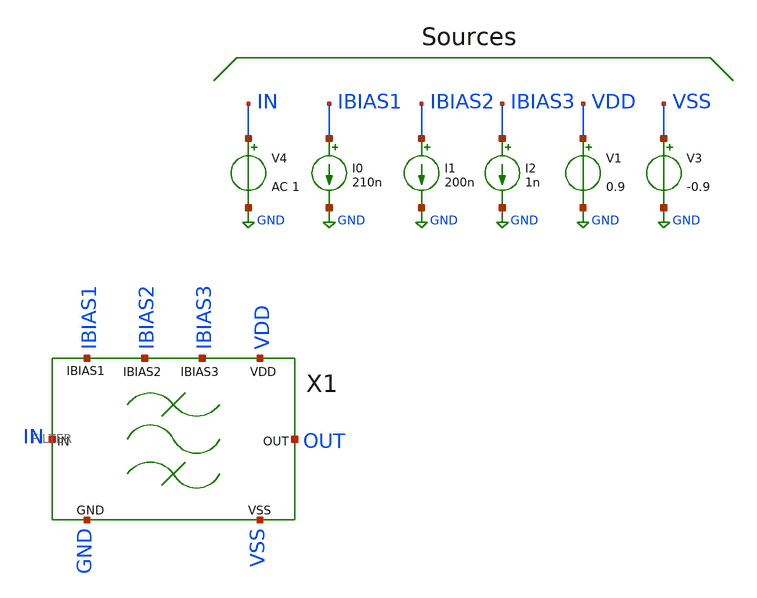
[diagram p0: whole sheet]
** sch_path: xschem/FILTER/FILTER_TB.sch
**.subckt FILTER_TB
I0 IBIAS1 GND 210n
V1 VDD GND 0.9
V4 IN GND AC 1
V3 VSS GND -0.9
I1 IBIAS2 GND 200n
I2 IBIAS3 GND 1n
X1 IBIAS1 VSS IBIAS2 GND IBIAS3 IN OUT VDD FILTER
**** begin user architecture code



*.include ~/OpenPDK/skywater-pdk/skywater-pdk/libraries/sky130_fd_pr/latest/cells/pfet_g5v0d10v5/sky130_fd_pr__pfet_g5v0d10v5__tt.corner.spice
*.include ~/OpenPDK/skywater-pdk/skywater-pdk/libraries/sky130_fd_pr/latest/cells/pfet_g5v0d10v5/sky130_fd_pr__pfet_g5v0d10v5__mismatch.corner.spice
*.include ~/OpenPDK/skywater-pdk/skywater-pdk/libraries/sky130_fd_pr/latest/cells/pfet_g5v0d10v5/sky130_fd_pr__nfet_g5v0d10v5__tt.corner.spice
*.include ~/OpenPDK/skywater-pdk/skywater-pdk/libraries/sky130_fd_pr/latest/cells/pfet_g5v0d10v5/sky130_fd_pr__nfet_g5v0d10v5__mismatch.corner.spice

.include /usr/share/pdk/sky130A/libs.ref/spi/sky130_fd_pr/sky130_fd_pr__nfet_01v8_lvt__tt.corner.spice
.include /usr/share/pdk/sky130A/libs.ref/spi/sky130_fd_pr/sky130_fd_pr__nfet_01v8_lvt__mismatch.corner.spice
.include /usr/share/pdk/sky130A/libs.ref/spi/sky130_fd_pr/sky130_fd_pr__pfet_01v8_lvt__tt.corner.spice
.include /usr/share/pdk/sky130A/libs.ref/spi/sky130_fd_pr/sky130_fd_pr__pfet_01v8_lvt__mismatch.corner.spice
*.include /usr/share/pdk/sky130A/libs.ref/spi/sky130_fd_pr/sky130_fd_pr__cap_mim_m3_1.model.spice



.include ~/OpenPDK/skywater-pdk/skywater-pdk/libraries/sky130_fd_pr/latest/models/all.spice
.include ~/OpenPDK/skywater-pdk/skywater-pdk/libraries/sky130_fd_pr/latest/models/sky130_fd_pr__model__r+c.model.spice
.include ~/OpenPDK/skywater-pdk/skywater-pdk/libraries/sky130_fd_pr/latest/models/r+c/res_typical__cap_typical.spice
.include ~/OpenPDK/skywater-pdk/skywater-pdk/libraries/sky130_fd_pr/latest/models/r+c/res_typical__cap_typical__lin.spice





.option gmin=1E-14

.control


******************************OP Simulation****************************
op
print OUT
*print MINUS1
*print MINUS2
***********************************************************************


******************************DC Simulation****************************
*dc V2 0.85 0.95 10u
*plot OUT
*plot deriv(OUT)
***********************************************************************


******************************AC Simulation****************************
ac dec 100 0.01 10000
plot db(OUT)
***********************************************************************


******************************Noise Simulation*************************
*set sqrnoise
*noise v(out) V4 dec 100 50m 100
*setplot noise1
*plot log(inoise_spectrum)
*plot onoise_spectrum

*print inoise_total
*print onoise_total
***********************************************************************


.endc


**** end user architecture code
**.ends
.GLOBAL GND
.end
